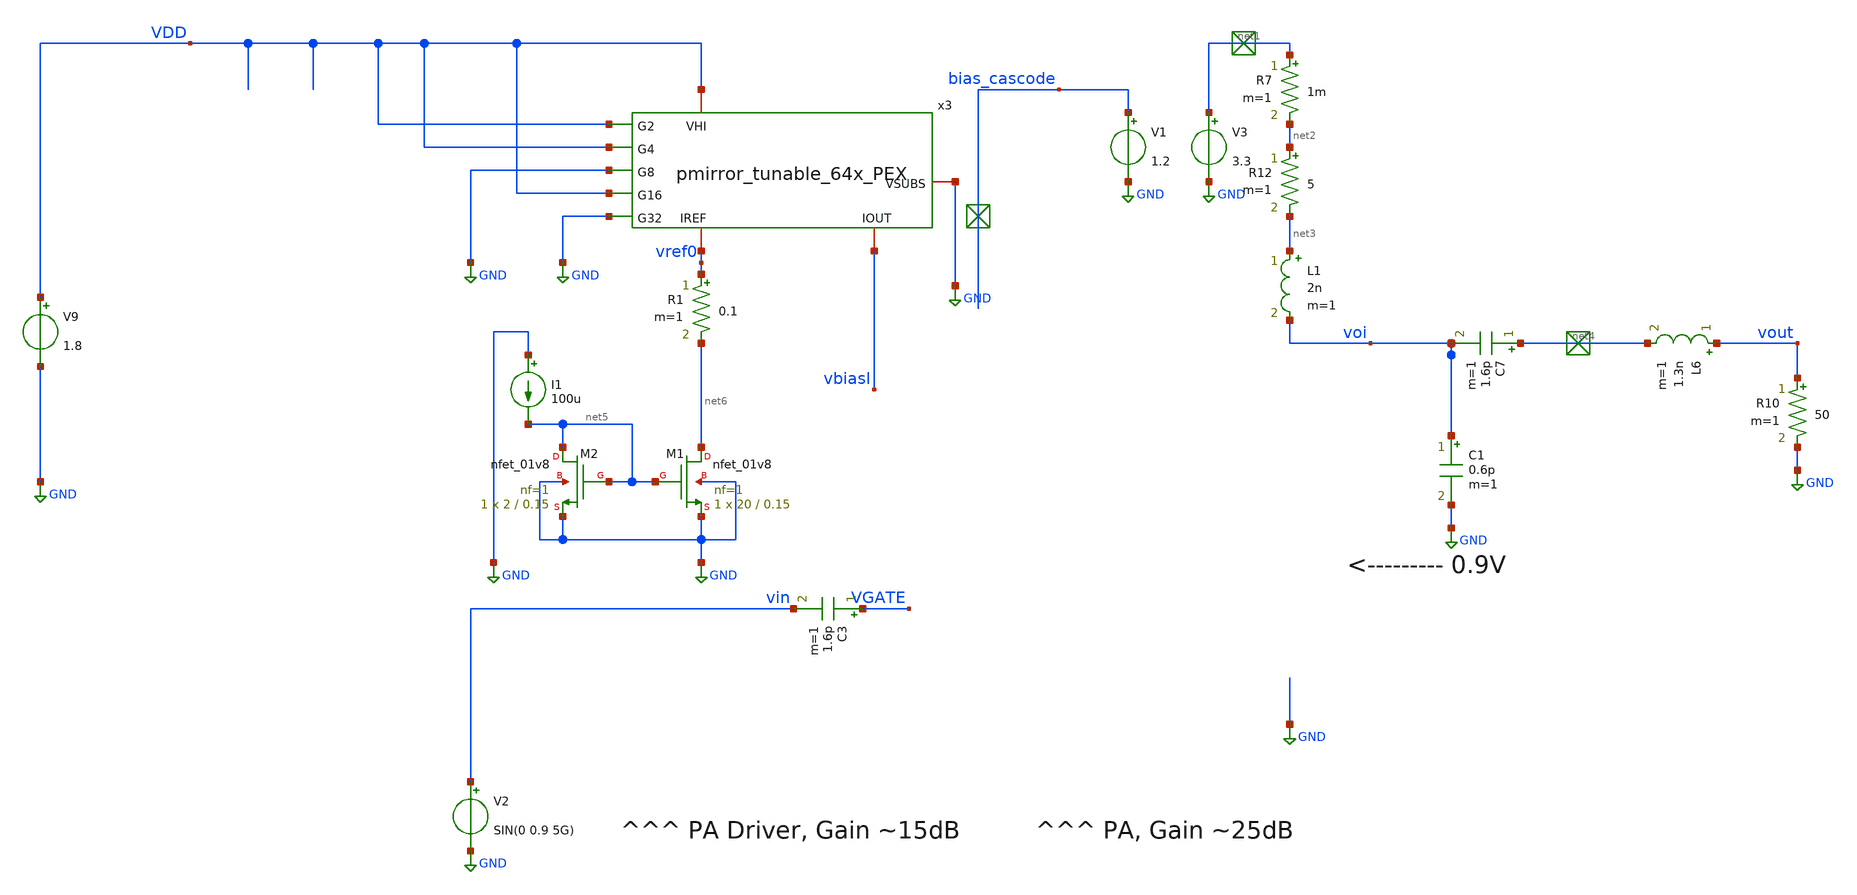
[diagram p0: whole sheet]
** sch_path: xschem/2stack_res_matching_newbias_PEX.sch
**.subckt 2stack_res_matching_newbias_PEX
V3 net1 GND 3.3
L1 net3 voi 2n m=1
L6 vout net4 1.3n m=1
C7 net4 voi 1.6p m=1
C1 voi GND 0.6p m=1
R7 net1 net2 1m m=1
R12 net2 net3 5 m=1
R10 vout GND 50 m=1
V1 bias_cascode GND 1.2
I1 GND net5 100u
V9 VDD GND 1.8
C3 VGATE vin 1.6p m=1
V2 vin GND SIN(0 0.9 5G)
XM1 net6 net5 GND GND sky130_fd_pr__nfet_01v8 L=0.15 W=20 nf=1 ad='int((nf+1)/2) * W/nf * 0.29' as='int((nf+2)/2) * W/nf * 0.29'
+ pd='2*int((nf+1)/2) * (W/nf + 0.29)' ps='2*int((nf+2)/2) * (W/nf + 0.29)' nrd='0.29 / W' nrs='0.29 / W'
+ sa=0 sb=0 sd=0 mult=1 m=1
XM2 net5 net5 GND GND sky130_fd_pr__nfet_01v8 L=0.15 W=2 nf=1 ad='int((nf+1)/2) * W/nf * 0.29' as='int((nf+2)/2) * W/nf * 0.29'
+ pd='2*int((nf+1)/2) * (W/nf + 0.29)' ps='2*int((nf+2)/2) * (W/nf + 0.29)' nrd='0.29 / W' nrs='0.29 / W'
+ sa=0 sb=0 sd=0 mult=1 m=1
R1 vref0 net6 0.1 m=1
x3 VDD VDD VDD GND GND vref0 vbiasl VDD GND pmirror_tunable_64x_PEX
**** begin user architecture code
.lib $::SKYWATER_MODELS/sky130.lib.spice tt
* .include $::PDKPATH/libs.ref/sky130_fd_sc_hvl/spice/sky130_fd_sc_hvl.spice


.subckt DUT IREF_L GND VBIAS_CAS INPUT OUTPUT

.subckt sky130_fd_pr__nfet_01v8_6H2JGK a_63_n800# a_n225_n800# a_111_822# a_n321_n800#  a_207_n888#
+ a_n369_n888# a_n33_n800# a_303_822# a_15_n888# a_n81_822# a_n177_n888#  a_159_n800# a_n515_n974# a_n273_822#
+ a_255_n800# a_n413_n800# a_351_n800# a_n129_n800#
X0 a_n129_n800# a_n177_n888# a_n225_n800# a_n515_n974# sky130_fd_pr__nfet_01v8 ad=2.64e+12p
+ pd=1.666e+07u as=2.64e+12p ps=1.666e+07u w=8e+06u l=150000u
X1 a_351_n800# a_303_822# a_255_n800# a_n515_n974# sky130_fd_pr__nfet_01v8 ad=2.48e+12p
+ pd=1.662e+07u as=2.64e+12p ps=1.666e+07u w=8e+06u l=150000u
X2 a_n33_n800# a_n81_822# a_n129_n800# a_n515_n974# sky130_fd_pr__nfet_01v8 ad=2.64e+12p
+ pd=1.666e+07u as=0p ps=0u w=8e+06u l=150000u
X3 a_255_n800# a_207_n888# a_159_n800# a_n515_n974# sky130_fd_pr__nfet_01v8 ad=0p pd=0u as=2.64e+12p
+ ps=1.666e+07u w=8e+06u l=150000u
X4 a_n321_n800# a_n369_n888# a_n413_n800# a_n515_n974# sky130_fd_pr__nfet_01v8 ad=2.64e+12p
+ pd=1.666e+07u as=2.48e+12p ps=1.662e+07u w=8e+06u l=150000u
X5 a_159_n800# a_111_822# a_63_n800# a_n515_n974# sky130_fd_pr__nfet_01v8 ad=0p pd=0u as=2.64e+12p
+ ps=1.666e+07u w=8e+06u l=150000u
X6 a_n225_n800# a_n273_822# a_n321_n800# a_n515_n974# sky130_fd_pr__nfet_01v8 ad=0p pd=0u as=0p
+ ps=0u w=8e+06u l=150000u
X7 a_63_n800# a_15_n888# a_n33_n800# a_n515_n974# sky130_fd_pr__nfet_01v8 ad=0p pd=0u as=0p ps=0u
+ w=8e+06u l=150000u
.ends

.subckt sky130_fd_pr__res_high_po_0p35_ZE2H5K a_n35_300# a_n165_n862# a_n35_n732#
X0 a_n35_n732# a_n35_300# a_n165_n862# sky130_fd_pr__res_high_po_0p35 l=3e+06u
.ends

.subckt sky130_fd_pr__nfet_03v3_nvt_EV757D a_977_n997# a_n1135_1127# a_603_n1927#  a_n2557_n909#
+ a_n1551_21# a_2241_n2015# a_n445_n997# a_2183_109# a_1235_109# a_n2083_109#  a_n977_1127# a_819_1039#
+ a_n1709_n997# a_n1135_109# a_n2025_n997# a_n1767_n909#  a_1235_n1927# a_n2557_1127# a_n1077_1039# a_n2083_n909#
+ a_n2499_n2015# a_1709_n1927#  a_2399_n997# a_n1235_n997# a_345_1039# a_n503_n909# a_n1767_1127# a_n1293_n909#
+  a_129_n909# a_2083_n2015# a_445_n1927# a_977_21# a_n2083_1127# a_n2499_1039# a_503_n997#  a_919_n1927#
+ a_187_21# a_n503_1127# a_n919_1039# a_1077_n1927# a_129_1127# a_n1293_1127#  a_1609_n997# a_1077_109#
+ a_n977_109# a_977_1039# a_29_n2015# a_n1867_n997# a_1609_21#  a_n445_1039# a_287_n1927# a_n2183_n997#
+ a_n1709_1039# a_2399_n2015# a_1551_n1927#  a_n603_n997# a_1451_21# a_n2025_1039# a_1135_n997# a_n661_n909#
+ a_n1393_n997# a_287_n909#  a_129_109# a_2399_1039# a_n1925_n909# a_n445_21# a_n1235_1039# a_n2241_n909#
+ a_n29_n1927#  a_761_n1927# a_661_n997# a_n661_1127# a_503_1039# a_1393_n1927# a_n2183_21# a_287_1127#
+  a_n1925_1127# a_n1451_n909# a_n2241_1127# a_1867_n1927# a_1767_n997# a_2083_n997#  a_1709_109# a_n2557_109#
+ a_n1609_109# a_1609_1039# a_n1867_21# a_n1451_1127# a_n1867_1039#  a_n2183_1039# a_n761_n997# a_1293_n997#
+ a_n1077_21# a_n2341_n997# a_n603_1039# a_919_n909#  a_1135_1039# a_n29_109# a_n1393_1039# a_n1135_n1927#
+ a_1551_109# a_n1451_109# a_345_21#  a_29_21# a_661_1039# a_n1609_n1927# a_n1551_n997# a_919_1127# a_445_n909#
+ a_n503_n1927#  a_n129_n2015# a_2499_109# a_n503_109# a_n2399_109# a_603_109# a_445_1127# a_1767_1039#
+  a_n1235_n2015# a_2083_21# a_2083_1039# a_n1709_n2015# a_1925_n997# a_n603_n2015#  a_2241_n997# a_n761_1039#
+ a_n345_n1927# a_1767_21# a_1293_1039# a_n603_21# a_1077_n909#  a_n819_n1927# a_2025_n1927# a_n2341_1039#
+ a_1451_n997# a_1393_109# a_n1293_109#  a_n1077_n2015# a_n1451_n1927# a_n2341_21# a_n1925_n1927# a_1077_1127#
+ a_n1551_1039#  a_2499_n909# a_n445_n2015# a_503_n2015# a_n2691_n2149# a_n187_n1927# a_n345_109#  a_n2499_21#
+ a_n919_n2015# a_445_109# a_603_n909# a_n1551_n2015# a_1135_n2015# a_2499_1127#  a_n1293_n1927# a_n1235_21#
+ a_1609_n2015# a_n1767_n1927# a_1925_1039# a_603_1127#  a_1709_n909# a_345_n2015# a_n661_n1927# a_2241_1039#
+ a_n287_n2015# a_2341_n1927#  a_2025_n909# a_819_n2015# a_n1925_109# a_503_21# a_n1393_n2015# a_1451_1039#
+ a_1709_1127#  a_1235_n909# a_n1867_n2015# a_2025_1127# a_2025_109# a_n187_109# a_n761_n2015# a_2241_21#
+  a_761_n909# a_187_n2015# a_287_109# a_2183_n1927# a_1235_1127# a_1451_n2015# a_n977_n1927#  a_2399_21#
+ a_1925_n2015# a_1925_21# a_761_1127# a_1867_n909# a_2183_n909# a_661_n2015#  a_1135_21# a_1867_109# a_n1767_109#
+ a_n29_n909# a_n919_21# a_1867_1127# a_1293_n2015#  a_n761_21# a_2183_1127# a_1393_n909# a_2499_n1927#
+ a_n129_21# a_1767_n2015# a_29_n997#  a_n819_109# a_n29_1127# a_919_109# a_1393_1127# a_n129_n997# a_977_n2015#
+ a_n187_n909#  a_n2025_n2015# a_187_n997# a_n661_109# a_n1393_21# a_n187_1127# a_761_109# a_819_21#  a_2341_n909#
+ a_661_21# a_n2241_n1927# a_29_1039# a_1551_n909# a_n2399_n909# a_2341_1127#  a_n287_n997# a_n819_n909#
+ a_n129_1039# a_1551_1127# a_n2399_1127# a_n2341_n2015#  a_819_n997# a_n2083_n1927# a_2341_109# a_n2241_109#
+ a_n819_1127# a_187_1039# a_n345_n909#  a_n2557_n1927# a_n1077_n997# a_n1609_n909# a_345_n997# a_1293_21#
+ a_n2499_n997#  a_n345_1127# a_129_n1927# a_n2025_21# a_n1609_1127# a_n2183_n2015# a_n1135_n909#  a_n919_n997#
+ a_n287_21# a_n977_n909# a_n2399_n1927# a_n287_1039# a_n1709_21#
X0 a_n29_1127# a_n129_1039# a_n187_1127# a_n2691_n2149# sky130_fd_pr__nfet_03v3_nvt ad=1.16e+12p
+ pd=8.58e+06u as=1.16e+12p ps=8.58e+06u w=4e+06u l=500000u
X1 a_603_1127# a_503_1039# a_445_1127# a_n2691_n2149# sky130_fd_pr__nfet_03v3_nvt ad=1.16e+12p
+ pd=8.58e+06u as=1.16e+12p ps=8.58e+06u w=4e+06u l=500000u
X2 a_n661_109# a_n761_21# a_n819_109# a_n2691_n2149# sky130_fd_pr__nfet_03v3_nvt ad=1.16e+12p
+ pd=8.58e+06u as=1.16e+12p ps=8.58e+06u w=4e+06u l=500000u
X3 a_n1293_n1927# a_n1393_n2015# a_n1451_n1927# a_n2691_n2149# sky130_fd_pr__nfet_03v3_nvt
+ ad=1.16e+12p pd=8.58e+06u as=1.16e+12p ps=8.58e+06u w=4e+06u l=500000u
X4 a_n661_n909# a_n761_n997# a_n819_n909# a_n2691_n2149# sky130_fd_pr__nfet_03v3_nvt ad=1.16e+12p
+ pd=8.58e+06u as=1.16e+12p ps=8.58e+06u w=4e+06u l=500000u
X5 a_n29_n1927# a_n129_n2015# a_n187_n1927# a_n2691_n2149# sky130_fd_pr__nfet_03v3_nvt ad=1.16e+12p
+ pd=8.58e+06u as=1.16e+12p ps=8.58e+06u w=4e+06u l=500000u
X6 a_129_109# a_29_21# a_n29_109# a_n2691_n2149# sky130_fd_pr__nfet_03v3_nvt ad=1.16e+12p
+ pd=8.58e+06u as=1.16e+12p ps=8.58e+06u w=4e+06u l=500000u
X7 a_1551_n1927# a_1451_n2015# a_1393_n1927# a_n2691_n2149# sky130_fd_pr__nfet_03v3_nvt ad=1.16e+12p
+ pd=8.58e+06u as=1.16e+12p ps=8.58e+06u w=4e+06u l=500000u
X8 a_n1609_n1927# a_n1709_n2015# a_n1767_n1927# a_n2691_n2149# sky130_fd_pr__nfet_03v3_nvt
+ ad=1.16e+12p pd=8.58e+06u as=1.16e+12p ps=8.58e+06u w=4e+06u l=500000u
X9 a_2183_n1927# a_2083_n2015# a_2025_n1927# a_n2691_n2149# sky130_fd_pr__nfet_03v3_nvt ad=1.16e+12p
+ pd=8.58e+06u as=1.16e+12p ps=8.58e+06u w=4e+06u l=500000u
X10 a_n187_109# a_n287_21# a_n345_109# a_n2691_n2149# sky130_fd_pr__nfet_03v3_nvt ad=1.16e+12p
+ pd=8.58e+06u as=1.16e+12p ps=8.58e+06u w=4e+06u l=500000u
X11 a_919_n909# a_819_n997# a_761_n909# a_n2691_n2149# sky130_fd_pr__nfet_03v3_nvt ad=1.16e+12p
+ pd=8.58e+06u as=1.16e+12p ps=8.58e+06u w=4e+06u l=500000u
X12 a_n187_n1927# a_n287_n2015# a_n345_n1927# a_n2691_n2149# sky130_fd_pr__nfet_03v3_nvt ad=0p pd=0u
+ as=1.16e+12p ps=8.58e+06u w=4e+06u l=500000u
X13 a_n1767_n1927# a_n1867_n2015# a_n1925_n1927# a_n2691_n2149# sky130_fd_pr__nfet_03v3_nvt ad=0p
+ pd=0u as=1.16e+12p ps=8.58e+06u w=4e+06u l=500000u
X14 a_2025_n909# a_1925_n997# a_1867_n909# a_n2691_n2149# sky130_fd_pr__nfet_03v3_nvt ad=1.16e+12p
+ pd=8.58e+06u as=1.16e+12p ps=8.58e+06u w=4e+06u l=500000u
X15 a_1235_1127# a_1135_1039# a_1077_1127# a_n2691_n2149# sky130_fd_pr__nfet_03v3_nvt ad=1.16e+12p
+ pd=8.58e+06u as=1.16e+12p ps=8.58e+06u w=4e+06u l=500000u
X16 a_n2399_n1927# a_n2499_n2015# a_n2557_n1927# a_n2691_n2149# sky130_fd_pr__nfet_03v3_nvt
+ ad=1.16e+12p pd=8.58e+06u as=1.16e+12p ps=8.58e+06u w=4e+06u l=500000u
X17 a_761_n909# a_661_n997# a_603_n909# a_n2691_n2149# sky130_fd_pr__nfet_03v3_nvt ad=0p pd=0u
+ as=1.16e+12p ps=8.58e+06u w=4e+06u l=500000u
X18 a_n187_n909# a_n287_n997# a_n345_n909# a_n2691_n2149# sky130_fd_pr__nfet_03v3_nvt ad=1.16e+12p
+ pd=8.58e+06u as=1.16e+12p ps=8.58e+06u w=4e+06u l=500000u
X19 a_n1135_1127# a_n1235_1039# a_n1293_1127# a_n2691_n2149# sky130_fd_pr__nfet_03v3_nvt
+ ad=1.16e+12p pd=8.58e+06u as=1.16e+12p ps=8.58e+06u w=4e+06u l=500000u
X20 a_2025_n1927# a_1925_n2015# a_1867_n1927# a_n2691_n2149# sky130_fd_pr__nfet_03v3_nvt ad=0p pd=0u
+ as=1.16e+12p ps=8.58e+06u w=4e+06u l=500000u
X21 a_n819_109# a_n919_21# a_n977_109# a_n2691_n2149# sky130_fd_pr__nfet_03v3_nvt ad=0p pd=0u
+ as=1.16e+12p ps=8.58e+06u w=4e+06u l=500000u
X22 a_2341_n909# a_2241_n997# a_2183_n909# a_n2691_n2149# sky130_fd_pr__nfet_03v3_nvt ad=1.16e+12p
+ pd=8.58e+06u as=1.16e+12p ps=8.58e+06u w=4e+06u l=500000u
X23 a_n2241_n909# a_n2341_n997# a_n2399_n909# a_n2691_n2149# sky130_fd_pr__nfet_03v3_nvt
+ ad=1.16e+12p pd=8.58e+06u as=1.16e+12p ps=8.58e+06u w=4e+06u l=500000u
X24 a_n345_109# a_n445_21# a_n503_109# a_n2691_n2149# sky130_fd_pr__nfet_03v3_nvt ad=0p pd=0u
+ as=1.16e+12p ps=8.58e+06u w=4e+06u l=500000u
X25 a_287_n909# a_187_n997# a_129_n909# a_n2691_n2149# sky130_fd_pr__nfet_03v3_nvt ad=1.16e+12p
+ pd=8.58e+06u as=1.16e+12p ps=8.58e+06u w=4e+06u l=500000u
X26 a_129_n1927# a_29_n2015# a_n29_n1927# a_n2691_n2149# sky130_fd_pr__nfet_03v3_nvt ad=1.16e+12p
+ pd=8.58e+06u as=0p ps=0u w=4e+06u l=500000u
X27 a_n503_109# a_n603_21# a_n661_109# a_n2691_n2149# sky130_fd_pr__nfet_03v3_nvt ad=0p pd=0u as=0p
+ ps=0u w=4e+06u l=500000u
X28 a_1393_n909# a_1293_n997# a_1235_n909# a_n2691_n2149# sky130_fd_pr__nfet_03v3_nvt ad=1.16e+12p
+ pd=8.58e+06u as=1.16e+12p ps=8.58e+06u w=4e+06u l=500000u
X29 a_n1293_n909# a_n1393_n997# a_n1451_n909# a_n2691_n2149# sky130_fd_pr__nfet_03v3_nvt
+ ad=1.16e+12p pd=8.58e+06u as=1.16e+12p ps=8.58e+06u w=4e+06u l=500000u
X30 a_1867_1127# a_1767_1039# a_1709_1127# a_n2691_n2149# sky130_fd_pr__nfet_03v3_nvt ad=1.16e+12p
+ pd=8.58e+06u as=1.16e+12p ps=8.58e+06u w=4e+06u l=500000u
X31 a_n1767_1127# a_n1867_1039# a_n1925_1127# a_n2691_n2149# sky130_fd_pr__nfet_03v3_nvt
+ ad=1.16e+12p pd=8.58e+06u as=1.16e+12p ps=8.58e+06u w=4e+06u l=500000u
X32 a_n29_109# a_n129_21# a_n187_109# a_n2691_n2149# sky130_fd_pr__nfet_03v3_nvt ad=0p pd=0u as=0p
+ ps=0u w=4e+06u l=500000u
X33 a_n2399_109# a_n2499_21# a_n2557_109# a_n2691_n2149# sky130_fd_pr__nfet_03v3_nvt ad=1.16e+12p
+ pd=8.58e+06u as=1.16e+12p ps=8.58e+06u w=4e+06u l=500000u
X34 a_445_n1927# a_345_n2015# a_287_n1927# a_n2691_n2149# sky130_fd_pr__nfet_03v3_nvt ad=1.16e+12p
+ pd=8.58e+06u as=1.16e+12p ps=8.58e+06u w=4e+06u l=500000u
X35 a_n2083_1127# a_n2183_1039# a_n2241_1127# a_n2691_n2149# sky130_fd_pr__nfet_03v3_nvt
+ ad=1.16e+12p pd=8.58e+06u as=1.16e+12p ps=8.58e+06u w=4e+06u l=500000u
X36 a_2183_1127# a_2083_1039# a_2025_1127# a_n2691_n2149# sky130_fd_pr__nfet_03v3_nvt ad=1.16e+12p
+ pd=8.58e+06u as=1.16e+12p ps=8.58e+06u w=4e+06u l=500000u
X37 a_1867_109# a_1767_21# a_1709_109# a_n2691_n2149# sky130_fd_pr__nfet_03v3_nvt ad=1.16e+12p
+ pd=8.58e+06u as=1.16e+12p ps=8.58e+06u w=4e+06u l=500000u
X38 a_1393_109# a_1293_21# a_1235_109# a_n2691_n2149# sky130_fd_pr__nfet_03v3_nvt ad=1.16e+12p
+ pd=8.58e+06u as=1.16e+12p ps=8.58e+06u w=4e+06u l=500000u
X39 a_n345_n909# a_n445_n997# a_n503_n909# a_n2691_n2149# sky130_fd_pr__nfet_03v3_nvt ad=0p pd=0u
+ as=1.16e+12p ps=8.58e+06u w=4e+06u l=500000u
X40 a_1077_109# a_977_21# a_919_109# a_n2691_n2149# sky130_fd_pr__nfet_03v3_nvt ad=1.16e+12p
+ pd=8.58e+06u as=1.16e+12p ps=8.58e+06u w=4e+06u l=500000u
X41 a_2499_n909# a_2399_n997# a_2341_n909# a_n2691_n2149# sky130_fd_pr__nfet_03v3_nvt ad=1.16e+12p
+ pd=8.58e+06u as=0p ps=0u w=4e+06u l=500000u
X42 a_n2083_109# a_n2183_21# a_n2241_109# a_n2691_n2149# sky130_fd_pr__nfet_03v3_nvt ad=1.16e+12p
+ pd=8.58e+06u as=1.16e+12p ps=8.58e+06u w=4e+06u l=500000u
X43 a_919_n1927# a_819_n2015# a_761_n1927# a_n2691_n2149# sky130_fd_pr__nfet_03v3_nvt ad=1.16e+12p
+ pd=8.58e+06u as=1.16e+12p ps=8.58e+06u w=4e+06u l=500000u
X44 a_n2399_n909# a_n2499_n997# a_n2557_n909# a_n2691_n2149# sky130_fd_pr__nfet_03v3_nvt ad=0p pd=0u
+ as=1.16e+12p ps=8.58e+06u w=4e+06u l=500000u
X45 a_2025_109# a_1925_21# a_1867_109# a_n2691_n2149# sky130_fd_pr__nfet_03v3_nvt ad=1.16e+12p
+ pd=8.58e+06u as=0p ps=0u w=4e+06u l=500000u
X46 a_n819_1127# a_n919_1039# a_n977_1127# a_n2691_n2149# sky130_fd_pr__nfet_03v3_nvt ad=1.16e+12p
+ pd=8.58e+06u as=1.16e+12p ps=8.58e+06u w=4e+06u l=500000u
X47 a_n1925_n1927# a_n2025_n2015# a_n2083_n1927# a_n2691_n2149# sky130_fd_pr__nfet_03v3_nvt ad=0p
+ pd=0u as=1.16e+12p ps=8.58e+06u w=4e+06u l=500000u
X48 a_1551_109# a_1451_21# a_1393_109# a_n2691_n2149# sky130_fd_pr__nfet_03v3_nvt ad=1.16e+12p
+ pd=8.58e+06u as=0p ps=0u w=4e+06u l=500000u
X49 a_129_n909# a_29_n997# a_n29_n909# a_n2691_n2149# sky130_fd_pr__nfet_03v3_nvt ad=0p pd=0u
+ as=1.16e+12p ps=8.58e+06u w=4e+06u l=500000u
X50 a_n661_1127# a_n761_1039# a_n819_1127# a_n2691_n2149# sky130_fd_pr__nfet_03v3_nvt ad=1.16e+12p
+ pd=8.58e+06u as=0p ps=0u w=4e+06u l=500000u
X51 a_1077_n1927# a_977_n2015# a_919_n1927# a_n2691_n2149# sky130_fd_pr__nfet_03v3_nvt ad=1.16e+12p
+ pd=8.58e+06u as=0p ps=0u w=4e+06u l=500000u
X52 a_1709_n909# a_1609_n997# a_1551_n909# a_n2691_n2149# sky130_fd_pr__nfet_03v3_nvt ad=1.16e+12p
+ pd=8.58e+06u as=1.16e+12p ps=8.58e+06u w=4e+06u l=500000u
X53 a_n1451_n1927# a_n1551_n2015# a_n1609_n1927# a_n2691_n2149# sky130_fd_pr__nfet_03v3_nvt ad=0p
+ pd=0u as=0p ps=0u w=4e+06u l=500000u
X54 a_n1609_n909# a_n1709_n997# a_n1767_n909# a_n2691_n2149# sky130_fd_pr__nfet_03v3_nvt
+ ad=1.16e+12p pd=8.58e+06u as=1.16e+12p ps=8.58e+06u w=4e+06u l=500000u
X55 a_n2083_n1927# a_n2183_n2015# a_n2241_n1927# a_n2691_n2149# sky130_fd_pr__nfet_03v3_nvt ad=0p
+ pd=0u as=1.16e+12p ps=8.58e+06u w=4e+06u l=500000u
X56 a_445_n909# a_345_n997# a_287_n909# a_n2691_n2149# sky130_fd_pr__nfet_03v3_nvt ad=1.16e+12p
+ pd=8.58e+06u as=0p ps=0u w=4e+06u l=500000u
X57 a_n2241_109# a_n2341_21# a_n2399_109# a_n2691_n2149# sky130_fd_pr__nfet_03v3_nvt ad=0p pd=0u
+ as=0p ps=0u w=4e+06u l=500000u
X58 a_761_109# a_661_21# a_603_109# a_n2691_n2149# sky130_fd_pr__nfet_03v3_nvt ad=1.16e+12p
+ pd=8.58e+06u as=1.16e+12p ps=8.58e+06u w=4e+06u l=500000u
X59 a_2341_n1927# a_2241_n2015# a_2183_n1927# a_n2691_n2149# sky130_fd_pr__nfet_03v3_nvt
+ ad=1.16e+12p pd=8.58e+06u as=0p ps=0u w=4e+06u l=500000u
X60 a_1551_n909# a_1451_n997# a_1393_n909# a_n2691_n2149# sky130_fd_pr__nfet_03v3_nvt ad=0p pd=0u
+ as=0p ps=0u w=4e+06u l=500000u
X61 a_n1451_n909# a_n1551_n997# a_n1609_n909# a_n2691_n2149# sky130_fd_pr__nfet_03v3_nvt ad=0p pd=0u
+ as=0p ps=0u w=4e+06u l=500000u
X62 a_n1925_n909# a_n2025_n997# a_n2083_n909# a_n2691_n2149# sky130_fd_pr__nfet_03v3_nvt
+ ad=1.16e+12p pd=8.58e+06u as=1.16e+12p ps=8.58e+06u w=4e+06u l=500000u
X63 a_919_1127# a_819_1039# a_761_1127# a_n2691_n2149# sky130_fd_pr__nfet_03v3_nvt ad=1.16e+12p
+ pd=8.58e+06u as=1.16e+12p ps=8.58e+06u w=4e+06u l=500000u
X64 a_2025_1127# a_1925_1039# a_1867_1127# a_n2691_n2149# sky130_fd_pr__nfet_03v3_nvt ad=0p pd=0u
+ as=0p ps=0u w=4e+06u l=500000u
X65 a_n345_n1927# a_n445_n2015# a_n503_n1927# a_n2691_n2149# sky130_fd_pr__nfet_03v3_nvt ad=0p pd=0u
+ as=1.16e+12p ps=8.58e+06u w=4e+06u l=500000u
X66 a_1709_109# a_1609_21# a_1551_109# a_n2691_n2149# sky130_fd_pr__nfet_03v3_nvt ad=0p pd=0u as=0p
+ ps=0u w=4e+06u l=500000u
X67 a_287_109# a_187_21# a_129_109# a_n2691_n2149# sky130_fd_pr__nfet_03v3_nvt ad=1.16e+12p
+ pd=8.58e+06u as=0p ps=0u w=4e+06u l=500000u
X68 a_n187_1127# a_n287_1039# a_n345_1127# a_n2691_n2149# sky130_fd_pr__nfet_03v3_nvt ad=0p pd=0u
+ as=1.16e+12p ps=8.58e+06u w=4e+06u l=500000u
X69 a_761_1127# a_661_1039# a_603_1127# a_n2691_n2149# sky130_fd_pr__nfet_03v3_nvt ad=0p pd=0u as=0p
+ ps=0u w=4e+06u l=500000u
X70 a_1235_109# a_1135_21# a_1077_109# a_n2691_n2149# sky130_fd_pr__nfet_03v3_nvt ad=0p pd=0u as=0p
+ ps=0u w=4e+06u l=500000u
X71 a_2341_1127# a_2241_1039# a_2183_1127# a_n2691_n2149# sky130_fd_pr__nfet_03v3_nvt ad=1.16e+12p
+ pd=8.58e+06u as=0p ps=0u w=4e+06u l=500000u
X72 a_n2241_1127# a_n2341_1039# a_n2399_1127# a_n2691_n2149# sky130_fd_pr__nfet_03v3_nvt ad=0p pd=0u
+ as=1.16e+12p ps=8.58e+06u w=4e+06u l=500000u
X73 a_n977_n909# a_n1077_n997# a_n1135_n909# a_n2691_n2149# sky130_fd_pr__nfet_03v3_nvt ad=1.16e+12p
+ pd=8.58e+06u as=1.16e+12p ps=8.58e+06u w=4e+06u l=500000u
X74 a_919_109# a_819_21# a_761_109# a_n2691_n2149# sky130_fd_pr__nfet_03v3_nvt ad=0p pd=0u as=0p
+ ps=0u w=4e+06u l=500000u
X75 a_n1925_109# a_n2025_21# a_n2083_109# a_n2691_n2149# sky130_fd_pr__nfet_03v3_nvt ad=1.16e+12p
+ pd=8.58e+06u as=0p ps=0u w=4e+06u l=500000u
X76 a_n819_n1927# a_n919_n2015# a_n977_n1927# a_n2691_n2149# sky130_fd_pr__nfet_03v3_nvt
+ ad=1.16e+12p pd=8.58e+06u as=1.16e+12p ps=8.58e+06u w=4e+06u l=500000u
X77 a_1077_n909# a_977_n997# a_919_n909# a_n2691_n2149# sky130_fd_pr__nfet_03v3_nvt ad=1.16e+12p
+ pd=8.58e+06u as=0p ps=0u w=4e+06u l=500000u
X78 a_445_109# a_345_21# a_287_109# a_n2691_n2149# sky130_fd_pr__nfet_03v3_nvt ad=1.16e+12p
+ pd=8.58e+06u as=0p ps=0u w=4e+06u l=500000u
X79 a_n503_n909# a_n603_n997# a_n661_n909# a_n2691_n2149# sky130_fd_pr__nfet_03v3_nvt ad=0p pd=0u
+ as=0p ps=0u w=4e+06u l=500000u
X80 a_287_1127# a_187_1039# a_129_1127# a_n2691_n2149# sky130_fd_pr__nfet_03v3_nvt ad=1.16e+12p
+ pd=8.58e+06u as=1.16e+12p ps=8.58e+06u w=4e+06u l=500000u
X81 a_n977_n1927# a_n1077_n2015# a_n1135_n1927# a_n2691_n2149# sky130_fd_pr__nfet_03v3_nvt ad=0p
+ pd=0u as=1.16e+12p ps=8.58e+06u w=4e+06u l=500000u
X82 a_1393_1127# a_1293_1039# a_1235_1127# a_n2691_n2149# sky130_fd_pr__nfet_03v3_nvt ad=1.16e+12p
+ pd=8.58e+06u as=0p ps=0u w=4e+06u l=500000u
X83 a_n1293_1127# a_n1393_1039# a_n1451_1127# a_n2691_n2149# sky130_fd_pr__nfet_03v3_nvt ad=0p pd=0u
+ as=1.16e+12p ps=8.58e+06u w=4e+06u l=500000u
X84 a_1235_n1927# a_1135_n2015# a_1077_n1927# a_n2691_n2149# sky130_fd_pr__nfet_03v3_nvt
+ ad=1.16e+12p pd=8.58e+06u as=0p ps=0u w=4e+06u l=500000u
X85 a_603_109# a_503_21# a_445_109# a_n2691_n2149# sky130_fd_pr__nfet_03v3_nvt ad=0p pd=0u as=0p
+ ps=0u w=4e+06u l=500000u
X86 a_603_n909# a_503_n997# a_445_n909# a_n2691_n2149# sky130_fd_pr__nfet_03v3_nvt ad=0p pd=0u as=0p
+ ps=0u w=4e+06u l=500000u
X87 a_n29_n909# a_n129_n997# a_n187_n909# a_n2691_n2149# sky130_fd_pr__nfet_03v3_nvt ad=0p pd=0u
+ as=0p ps=0u w=4e+06u l=500000u
X88 a_1393_n1927# a_1293_n2015# a_1235_n1927# a_n2691_n2149# sky130_fd_pr__nfet_03v3_nvt ad=0p pd=0u
+ as=0p ps=0u w=4e+06u l=500000u
X89 a_603_n1927# a_503_n2015# a_445_n1927# a_n2691_n2149# sky130_fd_pr__nfet_03v3_nvt ad=1.16e+12p
+ pd=8.58e+06u as=0p ps=0u w=4e+06u l=500000u
X90 a_1709_n1927# a_1609_n2015# a_1551_n1927# a_n2691_n2149# sky130_fd_pr__nfet_03v3_nvt
+ ad=1.16e+12p pd=8.58e+06u as=0p ps=0u w=4e+06u l=500000u
X91 a_n345_1127# a_n445_1039# a_n503_1127# a_n2691_n2149# sky130_fd_pr__nfet_03v3_nvt ad=0p pd=0u
+ as=1.16e+12p ps=8.58e+06u w=4e+06u l=500000u
X92 a_761_n1927# a_661_n2015# a_603_n1927# a_n2691_n2149# sky130_fd_pr__nfet_03v3_nvt ad=0p pd=0u
+ as=0p ps=0u w=4e+06u l=500000u
X93 a_n2399_1127# a_n2499_1039# a_n2557_1127# a_n2691_n2149# sky130_fd_pr__nfet_03v3_nvt ad=0p pd=0u
+ as=1.16e+12p ps=8.58e+06u w=4e+06u l=500000u
X94 a_2499_1127# a_2399_1039# a_2341_1127# a_n2691_n2149# sky130_fd_pr__nfet_03v3_nvt ad=1.16e+12p
+ pd=8.58e+06u as=0p ps=0u w=4e+06u l=500000u
X95 a_n1767_109# a_n1867_21# a_n1925_109# a_n2691_n2149# sky130_fd_pr__nfet_03v3_nvt ad=1.16e+12p
+ pd=8.58e+06u as=0p ps=0u w=4e+06u l=500000u
X96 a_1867_n1927# a_1767_n2015# a_1709_n1927# a_n2691_n2149# sky130_fd_pr__nfet_03v3_nvt ad=0p pd=0u
+ as=0p ps=0u w=4e+06u l=500000u
X97 a_n1293_109# a_n1393_21# a_n1451_109# a_n2691_n2149# sky130_fd_pr__nfet_03v3_nvt ad=1.16e+12p
+ pd=8.58e+06u as=1.16e+12p ps=8.58e+06u w=4e+06u l=500000u
X98 a_2499_n1927# a_2399_n2015# a_2341_n1927# a_n2691_n2149# sky130_fd_pr__nfet_03v3_nvt
+ ad=1.16e+12p pd=8.58e+06u as=0p ps=0u w=4e+06u l=500000u
X99 a_1235_n909# a_1135_n997# a_1077_n909# a_n2691_n2149# sky130_fd_pr__nfet_03v3_nvt ad=0p pd=0u
+ as=0p ps=0u w=4e+06u l=500000u
X100 a_n1135_n909# a_n1235_n997# a_n1293_n909# a_n2691_n2149# sky130_fd_pr__nfet_03v3_nvt ad=0p
+ pd=0u as=0p ps=0u w=4e+06u l=500000u
X101 a_129_1127# a_29_1039# a_n29_1127# a_n2691_n2149# sky130_fd_pr__nfet_03v3_nvt ad=0p pd=0u as=0p
+ ps=0u w=4e+06u l=500000u
X102 a_n1609_1127# a_n1709_1039# a_n1767_1127# a_n2691_n2149# sky130_fd_pr__nfet_03v3_nvt
+ ad=1.16e+12p pd=8.58e+06u as=0p ps=0u w=4e+06u l=500000u
X103 a_1709_1127# a_1609_1039# a_1551_1127# a_n2691_n2149# sky130_fd_pr__nfet_03v3_nvt ad=0p pd=0u
+ as=1.16e+12p ps=8.58e+06u w=4e+06u l=500000u
X104 a_445_1127# a_345_1039# a_287_1127# a_n2691_n2149# sky130_fd_pr__nfet_03v3_nvt ad=0p pd=0u
+ as=0p ps=0u w=4e+06u l=500000u
X105 a_n1451_109# a_n1551_21# a_n1609_109# a_n2691_n2149# sky130_fd_pr__nfet_03v3_nvt ad=0p pd=0u
+ as=1.16e+12p ps=8.58e+06u w=4e+06u l=500000u
X106 a_n2241_n1927# a_n2341_n2015# a_n2399_n1927# a_n2691_n2149# sky130_fd_pr__nfet_03v3_nvt ad=0p
+ pd=0u as=0p ps=0u w=4e+06u l=500000u
X107 a_n1925_1127# a_n2025_1039# a_n2083_1127# a_n2691_n2149# sky130_fd_pr__nfet_03v3_nvt ad=0p
+ pd=0u as=0p ps=0u w=4e+06u l=500000u
X108 a_n1451_1127# a_n1551_1039# a_n1609_1127# a_n2691_n2149# sky130_fd_pr__nfet_03v3_nvt ad=0p
+ pd=0u as=0p ps=0u w=4e+06u l=500000u
X109 a_1551_1127# a_1451_1039# a_1393_1127# a_n2691_n2149# sky130_fd_pr__nfet_03v3_nvt ad=0p pd=0u
+ as=0p ps=0u w=4e+06u l=500000u
X110 a_2499_109# a_2399_21# a_2341_109# a_n2691_n2149# sky130_fd_pr__nfet_03v3_nvt ad=1.16e+12p
+ pd=8.58e+06u as=1.16e+12p ps=8.58e+06u w=4e+06u l=500000u
X111 a_n977_109# a_n1077_21# a_n1135_109# a_n2691_n2149# sky130_fd_pr__nfet_03v3_nvt ad=0p pd=0u
+ as=1.16e+12p ps=8.58e+06u w=4e+06u l=500000u
X112 a_n503_n1927# a_n603_n2015# a_n661_n1927# a_n2691_n2149# sky130_fd_pr__nfet_03v3_nvt ad=0p
+ pd=0u as=1.16e+12p ps=8.58e+06u w=4e+06u l=500000u
X113 a_1867_n909# a_1767_n997# a_1709_n909# a_n2691_n2149# sky130_fd_pr__nfet_03v3_nvt ad=0p pd=0u
+ as=0p ps=0u w=4e+06u l=500000u
X114 a_n1767_n909# a_n1867_n997# a_n1925_n909# a_n2691_n2149# sky130_fd_pr__nfet_03v3_nvt ad=0p
+ pd=0u as=0p ps=0u w=4e+06u l=500000u
X115 a_287_n1927# a_187_n2015# a_129_n1927# a_n2691_n2149# sky130_fd_pr__nfet_03v3_nvt ad=0p pd=0u
+ as=0p ps=0u w=4e+06u l=500000u
X116 a_n977_1127# a_n1077_1039# a_n1135_1127# a_n2691_n2149# sky130_fd_pr__nfet_03v3_nvt ad=0p pd=0u
+ as=0p ps=0u w=4e+06u l=500000u
X117 a_2183_n909# a_2083_n997# a_2025_n909# a_n2691_n2149# sky130_fd_pr__nfet_03v3_nvt ad=0p pd=0u
+ as=0p ps=0u w=4e+06u l=500000u
X118 a_n1609_109# a_n1709_21# a_n1767_109# a_n2691_n2149# sky130_fd_pr__nfet_03v3_nvt ad=0p pd=0u
+ as=0p ps=0u w=4e+06u l=500000u
X119 a_1077_1127# a_977_1039# a_919_1127# a_n2691_n2149# sky130_fd_pr__nfet_03v3_nvt ad=0p pd=0u
+ as=0p ps=0u w=4e+06u l=500000u
X120 a_n661_n1927# a_n761_n2015# a_n819_n1927# a_n2691_n2149# sky130_fd_pr__nfet_03v3_nvt ad=0p
+ pd=0u as=0p ps=0u w=4e+06u l=500000u
X121 a_n2083_n909# a_n2183_n997# a_n2241_n909# a_n2691_n2149# sky130_fd_pr__nfet_03v3_nvt ad=0p
+ pd=0u as=0p ps=0u w=4e+06u l=500000u
X122 a_2183_109# a_2083_21# a_2025_109# a_n2691_n2149# sky130_fd_pr__nfet_03v3_nvt ad=1.16e+12p
+ pd=8.58e+06u as=0p ps=0u w=4e+06u l=500000u
X123 a_n1135_109# a_n1235_21# a_n1293_109# a_n2691_n2149# sky130_fd_pr__nfet_03v3_nvt ad=0p pd=0u
+ as=0p ps=0u w=4e+06u l=500000u
X124 a_n503_1127# a_n603_1039# a_n661_1127# a_n2691_n2149# sky130_fd_pr__nfet_03v3_nvt ad=0p pd=0u
+ as=0p ps=0u w=4e+06u l=500000u
X125 a_n1135_n1927# a_n1235_n2015# a_n1293_n1927# a_n2691_n2149# sky130_fd_pr__nfet_03v3_nvt ad=0p
+ pd=0u as=0p ps=0u w=4e+06u l=500000u
X126 a_2341_109# a_2241_21# a_2183_109# a_n2691_n2149# sky130_fd_pr__nfet_03v3_nvt ad=0p pd=0u as=0p
+ ps=0u w=4e+06u l=500000u
X127 a_n819_n909# a_n919_n997# a_n977_n909# a_n2691_n2149# sky130_fd_pr__nfet_03v3_nvt ad=0p pd=0u
+ as=0p ps=0u w=4e+06u l=500000u
.ends

.subckt RF_nfet_3v_dnwell_cascode D G2 G1 SB DNW VSUBS
Xsky130_fd_pr__nfet_03v3_nvt_EV757D_0 G1 D SB SB G2 G1 G2 SB SB D SB G1 G2 D G2 D  SB SB G2 D G2 D
+ G1 G2 G1 D D SB D G1 D G1 D G2 G1 SB G1 D G2 D D SB G1 D SB G1 G1  G2 G1 G2 SB G2 G2 G1 SB G2 G1 G2 G1
+ SB G2 SB D G1 SB G2 G2 SB SB D G1 SB G1 D G2  SB SB D SB SB G1 G1 D SB SB G1 G2 D G2 G2 G2 G1 G2 G2 G2
+ SB G1 SB G2 D SB D G1 G1  G1 SB G2 SB D D G2 SB D D SB D G1 G2 G1 G1 G2 G1 G2 G1 G2 SB G1 G1 G2 D D D
+ G2 G1  D SB G2 D G2 SB D G2 SB G2 G1 SB D SB G2 G2 D SB G2 G1 SB SB G2 G1 D G1 SB D G1  SB G1 G2 D D
+ G1 SB G1 G2 G1 D SB G2 D D D G2 G1 D G1 SB SB SB G1 SB G1 G1 G1 D SB  SB G1 G1 SB D SB G2 SB G1 G2 SB
+ D SB G2 G1 G1 D SB SB D G2 G1 D G2 G1 SB G2 D D  G1 D G1 SB G1 SB D D G2 D G2 SB D G2 G1 D D SB D G1
+ SB SB G2 SB G1 G1 G2 SB D G2  SB G2 D G2 G2 SB D G2 G2 sky130_fd_pr__nfet_03v3_nvt_EV757D
C0 D SB 132.51fF
C1 G1 SB 25.45fF
C2 G2 DNW 3.39fF
C3 D G1 19.92fF
C4 DNW SB 92.93fF
C5 G2 SB 27.04fF
C6 G1 DNW 2.85fF
C7 D G2 19.94fF
C8 SB VSUBS -3.31fF
C9 DNW VSUBS 112.06fF
C10 D VSUBS -2.56fF
C11 G1 VSUBS 3.47fF
C12 G2 VSUBS 3.41fF
.ends

.subckt sky130_fd_pr__rf_nfet_01v8_aM04_W5p00L0p15_notap G D S VSUBS
X0 D G S VSUBS sky130_fd_pr__nfet_01v8 ad=4.242e+12p pd=3.198e+07u as=2.828e+12p ps=2.132e+07u
+ w=5.05e+06u l=150000u
X1 D G S VSUBS sky130_fd_pr__nfet_01v8 ad=0p pd=0u as=0p ps=0u w=5.05e+06u l=150000u
X2 S G D VSUBS sky130_fd_pr__nfet_01v8 ad=0p pd=0u as=0p ps=0u w=5.05e+06u l=150000u
X3 S G D VSUBS sky130_fd_pr__nfet_01v8 ad=0p pd=0u as=0p ps=0u w=5.05e+06u l=150000u
C0 S D 6.34fF
.ends

.subckt RF_nfet_8xW5p0L0p15 G S SD
Xsky130_fd_pr__rf_nfet_01v8_aM04_W5p00L0p15_notap_0 G S SD S
+ sky130_fd_pr__rf_nfet_01v8_aM04_W5p00L0p15_notap
Xsky130_fd_pr__rf_nfet_01v8_aM04_W5p00L0p15_notap_1 G S SD S
+ sky130_fd_pr__rf_nfet_01v8_aM04_W5p00L0p15_notap
Xsky130_fd_pr__rf_nfet_01v8_aM04_W5p00L0p15_notap_2 G S SD S
+ sky130_fd_pr__rf_nfet_01v8_aM04_W5p00L0p15_notap
C0 G 0 2.12fF
.ends

.subckt RF_nfet_driver_64x8 G D SG
XRF_nfet_8xW5p0L0p15_9 G SG D RF_nfet_8xW5p0L0p15
XRF_nfet_8xW5p0L0p15_10 G SG D RF_nfet_8xW5p0L0p15
XRF_nfet_8xW5p0L0p15_11 G SG D RF_nfet_8xW5p0L0p15
XRF_nfet_8xW5p0L0p15_0 G SG D RF_nfet_8xW5p0L0p15
XRF_nfet_8xW5p0L0p15_1 G SG D RF_nfet_8xW5p0L0p15
XRF_nfet_8xW5p0L0p15_2 G SG D RF_nfet_8xW5p0L0p15
XRF_nfet_8xW5p0L0p15_3 G SG D RF_nfet_8xW5p0L0p15
XRF_nfet_8xW5p0L0p15_4 G SG D RF_nfet_8xW5p0L0p15
XRF_nfet_8xW5p0L0p15_5 G SG D RF_nfet_8xW5p0L0p15
XRF_nfet_8xW5p0L0p15_6 G SG D RF_nfet_8xW5p0L0p15
XRF_nfet_8xW5p0L0p15_7 G SG D RF_nfet_8xW5p0L0p15
XRF_nfet_8xW5p0L0p15_8 G SG D RF_nfet_8xW5p0L0p15
C0 D G 18.33fF
C1 D SG 24.68fF
C2 G SG 14.51fF
C3 D 0 -3.92fF
C4 SG 0 -25.16fF
C5 G 0 17.76fF
.ends

.subckt PA_core_1 DRAIN TOPBIAS_R GATE TOPBIAS_L MID VSUB
XRF_nfet_3v_dnwell_cascode_0 DRAIN RF_nfet_3v_dnwell_cascode_0/G2 RF_nfet_3v_dnwell_cascode_0/G1
+  MID VSUB VSUB RF_nfet_3v_dnwell_cascode
XRF_nfet_driver_64x8_0 GATE MID VSUB RF_nfet_driver_64x8
Xsky130_fd_pr__res_high_po_0p35_ZE2H5K_0 RF_nfet_3v_dnwell_cascode_0/G2 VSUB TOPBIAS_L
+  sky130_fd_pr__res_high_po_0p35_ZE2H5K
Xsky130_fd_pr__res_high_po_0p35_ZE2H5K_1 TOPBIAS_R VSUB RF_nfet_3v_dnwell_cascode_0/G1
+  sky130_fd_pr__res_high_po_0p35_ZE2H5K
C0 VSUB DRAIN 2.00fF
C1 VSUB MID 6.73fF
C2 VSUB 0 85.58fF
C3 GATE 0 17.76fF
C4 MID 0 -11.48fF
C5 DRAIN 0 -2.02fF
C6 RF_nfet_3v_dnwell_cascode_0/G1 0 4.12fF
C7 RF_nfet_3v_dnwell_cascode_0/G2 0 4.07fF
.ends

* PORTS:
* IREF_L, GND, INPUT, OUTPUT, VGATE_CAS


Xsky130_fd_pr__nfet_01v8_6H2JGK_0 IREF_L GND IREF_L IREF_L IREF_L IREF_L GND IREF_L  IREF_L IREF_L
+ IREF_L GND GND IREF_L IREF_L GND GND IREF_L sky130_fd_pr__nfet_01v8_6H2JGK
Xsky130_fd_pr__res_high_po_0p35_ZE2H5K_0 IREF_L GND INPUT sky130_fd_pr__res_high_po_0p35_ZE2H5K
XPA_core_1_0 OUTPUT VGATE_CAS INPUT VGATE_CAS PA_core_1_0/MID GND PA_core_1
X0 VGATE_CAS GND sky130_fd_pr__cap_mim_m3_2 l=1.6e+07u w=1.9e+07u
X1 GND VGATE_CAS sky130_fd_pr__cap_mim_m3_1 l=1.6e+07u w=1.9e+07u
X2 IREF_L GND sky130_fd_pr__cap_mim_m3_2 l=1.55e+07u w=2.25e+07u
X3 GND IREF_L sky130_fd_pr__cap_mim_m3_1 l=1.55e+07u w=2.25e+07u
C0 m5_n1000_18400# IREF_L 7.66fF
C1 VGATE_CAS GND 57.37fF
C2 GND IREF_L 84.58fF
C3 OUTPUT VGATE_CAS 4.71fF
C4 INPUT IREF_L 2.32fF
C8 VGATE_CAS 0 11.90fF
C10 INPUT 0 32.79fF
C12 OUTPUT 0 67.83fF
C13 PA_core_1_0/RF_nfet_3v_dnwell_cascode_0/G1 0 4.12fF
C14 PA_core_1_0/RF_nfet_3v_dnwell_cascode_0/G2 0 4.07fF
C15 IREF_L 0 16.35fF
.ends

XDUT vbiasl GND bias_cascode VGATE voi DUT

.options savecurrents
* XMU_0 gu voi mid mid rf_nfet_6xaM02_extracted
* XMU_1 gu voi mid mid rf_nfet_6xaM02_extracted
* XMU_2 gu voi mid mid rf_nfet_6xaM02_extracted
* XMU_3 gu voi mid mid rf_nfet_6xaM02_extracted
* XMU_4 gu voi mid mid rf_nfet_6xaM02_extracted
* XMU_5 gu voi mid mid rf_nfet_6xaM02_extracted
* XMD_0 gd mid gnd gnd rf_nfet_6xaM02_extracted
* XMD_1 gd mid gnd gnd rf_nfet_6xaM02_extracted
* XMD_2 gd mid gnd gnd rf_nfet_6xaM02_extracted
* XMD_3 gd mid gnd gnd rf_nfet_6xaM02_extracted
* XMD_4 gd mid gnd gnd rf_nfet_6xaM02_extracted
* XMD_5 gd mid gnd gnd rf_nfet_6xaM02_extracted
.tran 10ps 40ns
* .sp dec 1000 1e9 10e9 1
* .dc I1 0 10m 0.1m
.control
run
display
* plot @r5[i]
* let zout=@rload[r]
* let zin=50
* plot voi
* plot vout
* plot @c1[i]

plot vbiasl
plot @l1[i]


* meas TRAN vout_rms rms v(vout)
* meas TRAN isp_hi_avg  avg @r7[i]
* meas TRAN isp_mid_avg avg @r9[i]
* meas TRAN vin_rms rms v(vin)
* meas TRAN isp_1p8_avg avg @rsense2[i]
* let psp_rms  = isp_hi_avg*3.6 + isp_mid_avg*2.2
* let pout_rms = vout_rms^2/zout
* let pin_rms  = vin_rms^2/zin
* print psp_rms
* print ((pout_rms-pin_rms)/psp_rms)*100
* print 10*log10(pout_rms*1000)

* plot gd vmid voi vout

* let pout = mag(@rload[i]*vout)
* let poutdbm = log10((pout/(1e-3))*10
* plot pout

.endc


**** end user architecture code
**.ends

* expanding   symbol:  pmirror_tunable_64x_PEX.sym # of pins=9
** sym_path: xschem/pmirror_tunable_64x_PEX.sym
** sch_path: xschem/pmirror_tunable_64x_PEX.sch
.subckt pmirror_tunable_64x_PEX VHI G2 G4 VSUBS G8 IREF IOUT G16 G32
*.ipin G2
*.ipin G4
*.ipin G8
*.ipin G16
*.ipin G32
*.iopin VHI
*.iopin VSUBS
*.iopin IREF
*.iopin IOUT
**** begin user architecture code

* SPICE3 file created from pmirror_pfet_64x_complete.ext - technology: sky130B
X0 pmirror_pfet_64x_flat_0/G32 IREF VSUBS sky130_fd_pr__res_xhigh_po_0p35 l=500000u
X1 pmirror_pfet_64x_flat_0/G4  IREF VSUBS sky130_fd_pr__res_xhigh_po_0p35 l=500000u
X2 pmirror_pfet_64x_flat_0/G8  IREF VSUBS sky130_fd_pr__res_xhigh_po_0p35 l=500000u
X3 pmirror_pfet_64x_flat_0/G2  IREF VSUBS sky130_fd_pr__res_xhigh_po_0p35 l=500000u
X5 pmirror_pfet_64x_flat_0/G16 IREF VSUBS sky130_fd_pr__res_xhigh_po_0p35 l=500000u

X7 VHI pmirror_pfet_64x_flat_0/G32 IOUT VHI sky130_fd_pr__pfet_01v8 ad=0p pd=0u as=0p ps=0u w=1e+06u
+ l=300000u
X8 IOUT pmirror_pfet_64x_flat_0/G32 VHI VHI sky130_fd_pr__pfet_01v8 ad=0p pd=0u as=0p ps=0u w=1e+06u
+ l=300000u
X11 IOUT pmirror_pfet_64x_flat_0/G32 VHI VHI sky130_fd_pr__pfet_01v8 ad=0p pd=0u as=0p ps=0u
+ w=1e+06u l=300000u
X16 VHI pmirror_pfet_64x_flat_0/G32 IOUT VHI sky130_fd_pr__pfet_01v8 ad=0p pd=0u as=0p ps=0u
+ w=1e+06u l=300000u
X17 VHI pmirror_pfet_64x_flat_0/G32 IOUT VHI sky130_fd_pr__pfet_01v8 ad=0p pd=0u as=0p ps=0u
+ w=1e+06u l=300000u
X18 VHI pmirror_pfet_64x_flat_0/G32 IOUT VHI sky130_fd_pr__pfet_01v8 ad=0p pd=0u as=0p ps=0u
+ w=1e+06u l=300000u
X21 IOUT pmirror_pfet_64x_flat_0/G32 VHI VHI sky130_fd_pr__pfet_01v8 ad=0p pd=0u as=0p ps=0u
+ w=1e+06u l=300000u
X22 IOUT pmirror_pfet_64x_flat_0/G32 VHI VHI sky130_fd_pr__pfet_01v8 ad=0p pd=0u as=0p ps=0u
+ w=1e+06u l=300000u
X27 IOUT pmirror_pfet_64x_flat_0/G32 VHI VHI sky130_fd_pr__pfet_01v8 ad=1p pd=0u as=0p ps=0u
+ w=1e+06u l=300000u
X28 IOUT pmirror_pfet_64x_flat_0/G32 VHI VHI sky130_fd_pr__pfet_01v8 ad=0p pd=0u as=0p ps=0u
+ w=1e+06u l=300000u
X29 VHI pmirror_pfet_64x_flat_0/G32 IOUT VHI sky130_fd_pr__pfet_01v8 ad=0p pd=0u as=0p ps=0u
+ w=1e+06u l=300000u
X25 VHI pmirror_pfet_64x_flat_0/G32 IOUT VHI sky130_fd_pr__pfet_01v8 ad=0p pd=0u as=0p ps=0u
+ w=1e+06u l=300000u
X35 VHI pmirror_pfet_64x_flat_0/G32 IOUT VHI sky130_fd_pr__pfet_01v8 ad=0p pd=0u as=0p ps=0u
+ w=1e+06u l=300000u
X38 VHI pmirror_pfet_64x_flat_0/G32 IOUT VHI sky130_fd_pr__pfet_01v8 ad=0p pd=0u as=0p ps=0u
+ w=1e+06u l=300000u
X41 VHI pmirror_pfet_64x_flat_0/G32 IOUT VHI sky130_fd_pr__pfet_01v8 ad=0p pd=0u as=0p ps=0u
+ w=1e+06u l=300000u
X43 IOUT pmirror_pfet_64x_flat_0/G32 VHI VHI sky130_fd_pr__pfet_01v8 ad=0p pd=0u as=0p ps=0u
+ w=1e+06u l=300000u
X44 IOUT pmirror_pfet_64x_flat_0/G32 VHI VHI sky130_fd_pr__pfet_01v8 ad=0p pd=0u as=0p ps=0u
+ w=1e+06u l=300000u
X46 VHI pmirror_pfet_64x_flat_0/G32 IOUT VHI sky130_fd_pr__pfet_01v8 ad=0p pd=0u as=0p ps=0u
+ w=1e+06u l=300000u
X54 VHI pmirror_pfet_64x_flat_0/G32 IOUT VHI sky130_fd_pr__pfet_01v8 ad=0p pd=0u as=0p ps=0u
+ w=1e+06u l=300000u
X55 IOUT pmirror_pfet_64x_flat_0/G32 VHI VHI sky130_fd_pr__pfet_01v8 ad=0p pd=0u as=0p ps=0u
+ w=1e+06u l=300000u
X56 IOUT pmirror_pfet_64x_flat_0/G32 VHI VHI sky130_fd_pr__pfet_01v8 ad=0p pd=0u as=0p ps=0u
+ w=1e+06u l=300000u
X60 IOUT pmirror_pfet_64x_flat_0/G32 VHI VHI sky130_fd_pr__pfet_01v8 ad=0p pd=0u as=0p ps=0u
+ w=1e+06u l=300000u
X61 IOUT pmirror_pfet_64x_flat_0/G32 VHI VHI sky130_fd_pr__pfet_01v8 ad=0p pd=0u as=0p ps=0u
+ w=1e+06u l=300000u
X62 VHI pmirror_pfet_64x_flat_0/G32 IOUT VHI sky130_fd_pr__pfet_01v8 ad=0p pd=0u as=0p ps=0u
+ w=1e+06u l=300000u
X67 IOUT pmirror_pfet_64x_flat_0/G32 VHI VHI sky130_fd_pr__pfet_01v8 ad=0p pd=0u as=0p ps=0u
+ w=1e+06u l=300000u
X68 IOUT pmirror_pfet_64x_flat_0/G32 VHI VHI sky130_fd_pr__pfet_01v8 ad=0p pd=0u as=0p ps=0u
+ w=1e+06u l=300000u
X50 VHI pmirror_pfet_64x_flat_0/G32 IOUT VHI sky130_fd_pr__pfet_01v8 ad=0p pd=0u as=0p ps=0u
+ w=1e+06u l=300000u
X73 VHI pmirror_pfet_64x_flat_0/G32 IOUT VHI sky130_fd_pr__pfet_01v8 ad=0p pd=0u as=0p ps=0u
+ w=1e+06u l=300000u
X74 IOUT pmirror_pfet_64x_flat_0/G32 VHI VHI sky130_fd_pr__pfet_01v8 ad=0p pd=0u as=0p ps=0u
+ w=1e+06u l=300000u
X75 IOUT pmirror_pfet_64x_flat_0/G32 VHI VHI sky130_fd_pr__pfet_01v8 ad=0p pd=0u as=0p ps=0u
+ w=1e+06u l=300000u
X69 VHI pmirror_pfet_64x_flat_0/G32 IOUT VHI sky130_fd_pr__pfet_01v8 ad=0p pd=0u as=0p ps=0u
+ w=1e+06u l=300000u
X81 VHI pmirror_pfet_64x_flat_0/G32 IOUT VHI sky130_fd_pr__pfet_01v8 ad=0p pd=0u as=0p ps=0u
+ w=1e+06u l=300000u

X49 VHI VHI IOUT VHI sky130_fd_pr__pfet_01v8 ad=0p pd=0u as=0p ps=0u w=1e+06u l=300000u
X79 IREF IREF VHI VHI sky130_fd_pr__pfet_01v8 ad=0p pd=0u as=0p ps=0u w=1e+06u l=300000u

X6 IOUT pmirror_pfet_64x_flat_0/G16 VHI VHI sky130_fd_pr__pfet_01v8 ad=0p pd=0u as=0p ps=0u w=1e+06u
+ l=300000u
X9 VHI pmirror_pfet_64x_flat_0/G16 IOUT VHI sky130_fd_pr__pfet_01v8 ad=0p pd=0u as=0p ps=0u w=1e+06u
+ l=300000u
X10 IOUT pmirror_pfet_64x_flat_0/G16 VHI VHI sky130_fd_pr__pfet_01v8 ad=0p pd=0u as=0p ps=0u
+ w=1e+06u l=300000u
X19 IOUT pmirror_pfet_64x_flat_0/G16 VHI VHI sky130_fd_pr__pfet_01v8 ad=0p pd=0u as=0p ps=0u
+ w=1e+06u l=300000u
X20 IOUT pmirror_pfet_64x_flat_0/G16 VHI VHI sky130_fd_pr__pfet_01v8 ad=0p pd=0u as=0p ps=0u
+ w=1e+06u l=300000u
X26 VHI pmirror_pfet_64x_flat_0/G16 IOUT VHI sky130_fd_pr__pfet_01v8 ad=0p pd=0u as=0p ps=0u
+ w=1e+06u l=300000u
X30 IOUT pmirror_pfet_64x_flat_0/G16 VHI VHI sky130_fd_pr__pfet_01v8 ad=0p pd=0u as=0p ps=0u
+ w=1e+06u l=300000u
X33 IOUT pmirror_pfet_64x_flat_0/G16 VHI VHI sky130_fd_pr__pfet_01v8 ad=0p pd=0u as=0p ps=0u
+ w=1e+06u l=300000u
X36 VHI pmirror_pfet_64x_flat_0/G16 IOUT VHI sky130_fd_pr__pfet_01v8 ad=0p pd=0u as=0p ps=0u
+ w=1e+06u l=300000u
X45 VHI pmirror_pfet_64x_flat_0/G16 IOUT VHI sky130_fd_pr__pfet_01v8 ad=0p pd=0u as=0p ps=0u
+ w=1e+06u l=300000u
X53 VHI pmirror_pfet_64x_flat_0/G16 IOUT VHI sky130_fd_pr__pfet_01v8 ad=0p pd=0u as=0p ps=0u
+ w=1e+06u l=300000u
X57 VHI pmirror_pfet_64x_flat_0/G16 IOUT VHI sky130_fd_pr__pfet_01v8 ad=0p pd=0u as=0p ps=0u
+ w=1e+06u l=300000u
X58 VHI pmirror_pfet_64x_flat_0/G16 IOUT VHI sky130_fd_pr__pfet_01v8 ad=0p pd=0u as=0p ps=0u
+ w=1e+06u l=300000u
X65 VHI pmirror_pfet_64x_flat_0/G16 IOUT VHI sky130_fd_pr__pfet_01v8 ad=0p pd=0u as=0p ps=0u
+ w=1e+06u l=300000u
X82 IOUT pmirror_pfet_64x_flat_0/G16 VHI VHI sky130_fd_pr__pfet_01v8 ad=0p pd=0u as=0p ps=0u
+ w=1e+06u l=300000u
X83 IOUT pmirror_pfet_64x_flat_0/G16 VHI VHI sky130_fd_pr__pfet_01v8 ad=0p pd=0u as=0p ps=0u
+ w=1e+06u l=300000u

X14 IOUT pmirror_pfet_64x_flat_0/G8 VHI VHI sky130_fd_pr__pfet_01v8 ad=0p pd=0u as=0p ps=0u w=1e+06u
+ l=300000u
X23 VHI pmirror_pfet_64x_flat_0/G8 IOUT VHI sky130_fd_pr__pfet_01v8 ad=0p pd=0u as=0p ps=0u w=1e+06u
+ l=300000u
X31 VHI pmirror_pfet_64x_flat_0/G8 IOUT VHI sky130_fd_pr__pfet_01v8 ad=0p pd=0u as=0p ps=0u w=1e+06u
+ l=300000u
X32 VHI pmirror_pfet_64x_flat_0/G8 IOUT VHI sky130_fd_pr__pfet_01v8 ad=0p pd=0u as=0p ps=0u w=1e+06u
+ l=300000u
X42 VHI pmirror_pfet_64x_flat_0/G8 IOUT VHI sky130_fd_pr__pfet_01v8 ad=0p pd=0u as=0p ps=0u w=1e+06u
+ l=300000u
X72 IOUT pmirror_pfet_64x_flat_0/G8 VHI VHI sky130_fd_pr__pfet_01v8 ad=0p pd=0u as=0p ps=0u w=1e+06u
+ l=300000u
X80 IOUT pmirror_pfet_64x_flat_0/G8 VHI VHI sky130_fd_pr__pfet_01v8 ad=0p pd=0u as=0p ps=0u w=1e+06u
+ l=300000u
X84 IOUT pmirror_pfet_64x_flat_0/G8 VHI VHI sky130_fd_pr__pfet_01v8 ad=0p pd=0u as=0p ps=0u w=1e+06u
+ l=300000u

X85 IOUT pmirror_pfet_64x_flat_0/G4 VHI VHI sky130_fd_pr__pfet_01v8 ad=0p pd=0u as=0p ps=0u w=1e+06u
+ l=300000u
X39 VHI pmirror_pfet_64x_flat_0/G4 IOUT VHI sky130_fd_pr__pfet_01v8 ad=0p pd=0u as=0p ps=0u w=1e+06u
+ l=300000u
X40 VHI pmirror_pfet_64x_flat_0/G4 IOUT VHI sky130_fd_pr__pfet_01v8 ad=0p pd=0u as=0p ps=0u w=1e+06u
+ l=300000u
X70 IOUT pmirror_pfet_64x_flat_0/G4 VHI VHI sky130_fd_pr__pfet_01v8 ad=0p pd=0u as=0p ps=0u w=1e+06u
+ l=300000u

X48 VHI pmirror_pfet_64x_flat_0/G2 IOUT VHI sky130_fd_pr__pfet_01v8 ad=0p pd=0u as=0p ps=0u w=1e+06u
+ l=300000u
X15 IOUT pmirror_pfet_64x_flat_0/G2 VHI VHI sky130_fd_pr__pfet_01v8 ad=0p pd=0u as=0p ps=0u w=1e+06u
+ l=300000u

X86 VHI G32 pmirror_pfet_64x_flat_0/G32 VHI sky130_fd_pr__pfet_01v8 ad=0p pd=0u as=0p ps=0u
+ w=30e+06u l=150000u
X87 VHI G16 pmirror_pfet_64x_flat_0/G16 VHI sky130_fd_pr__pfet_01v8 ad=0p pd=0u as=0p ps=0u
+ w=30e+06u l=150000u
X88 VHI G2 pmirror_pfet_64x_flat_0/G2 VHI sky130_fd_pr__pfet_01v8 ad=0p pd=0u as=0p ps=0u w=30e+06u
+ l=150000u
X89 VHI G4 pmirror_pfet_64x_flat_0/G4 VHI sky130_fd_pr__pfet_01v8 ad=0p pd=0u as=0p ps=0u w=30e+06u
+ l=150000u
X90 VHI G8 pmirror_pfet_64x_flat_0/G8 VHI sky130_fd_pr__pfet_01v8 ad=0p pd=0u as=0p ps=0u w=30e+06u
+ l=150000u

C0 VHI pmirror_pfet_64x_flat_0/G8 10.15fF
C1 pmirror_pfet_64x_flat_0/G16 IOUT 2.36fF
C2 pmirror_pfet_64x_flat_0/G4 VHI 4.30fF
C3 pmirror_pfet_64x_flat_0/G2 IREF 2.13fF
C4 pmirror_pfet_64x_flat_0/G16 pmirror_pfet_64x_flat_0/G8 4.66fF
C5 pmirror_pfet_64x_flat_0/G4 pmirror_pfet_64x_flat_0/G8 3.24fF
C6 pmirror_pfet_64x_flat_0/G2 VHI 4.48fF
C7 pmirror_pfet_64x_flat_0/G4 pmirror_pfet_64x_flat_0/G2 2.55fF
C8 VHI IREF 4.53fF
C9 VHI pmirror_pfet_64x_flat_0/G32 15.40fF
C10 IOUT pmirror_pfet_64x_flat_0/G32 5.39fF
C11 pmirror_pfet_64x_flat_0/G16 pmirror_pfet_64x_flat_0/G32 3.74fF
C12 VHI IOUT 24.04fF
C13 pmirror_pfet_64x_flat_0/G16 VHI 4.93fF
C14 VHI VSUBS 46.10fF


**** end user architecture code
.ends

.GLOBAL GND
.end
